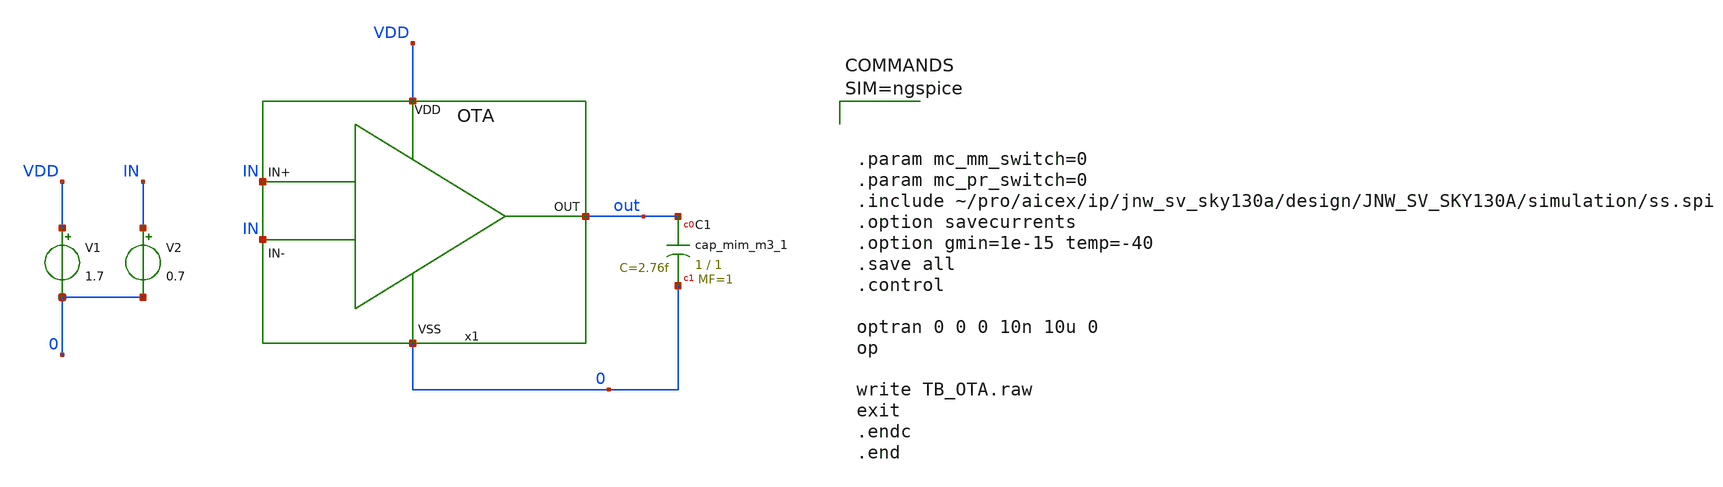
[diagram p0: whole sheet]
** sch_path: design/JNW_GR06_SKY130A/TB_OTA.sch
**.subckt TB_OTA
x1 VDD IN IN out 0 OTA
V1 VDD 0 1.7
V2 IN 0 0.7
XC1 out 0 sky130_fd_pr__cap_mim_m3_1 W=1 L=1 MF=1 m=1
**** begin user architecture code




.param mc_mm_switch=0
.param mc_pr_switch=0
.include ~/pro/aicex/ip/jnw_sv_sky130a/design/JNW_SV_SKY130A/simulation/ss.spi
.option savecurrents
.option gmin=1e-15 temp=-40
.save all
.control

optran 0 0 0 10n 10u 0
op

write TB_OTA.raw
exit
.endc
.end



**** end user architecture code
**.ends
.end
